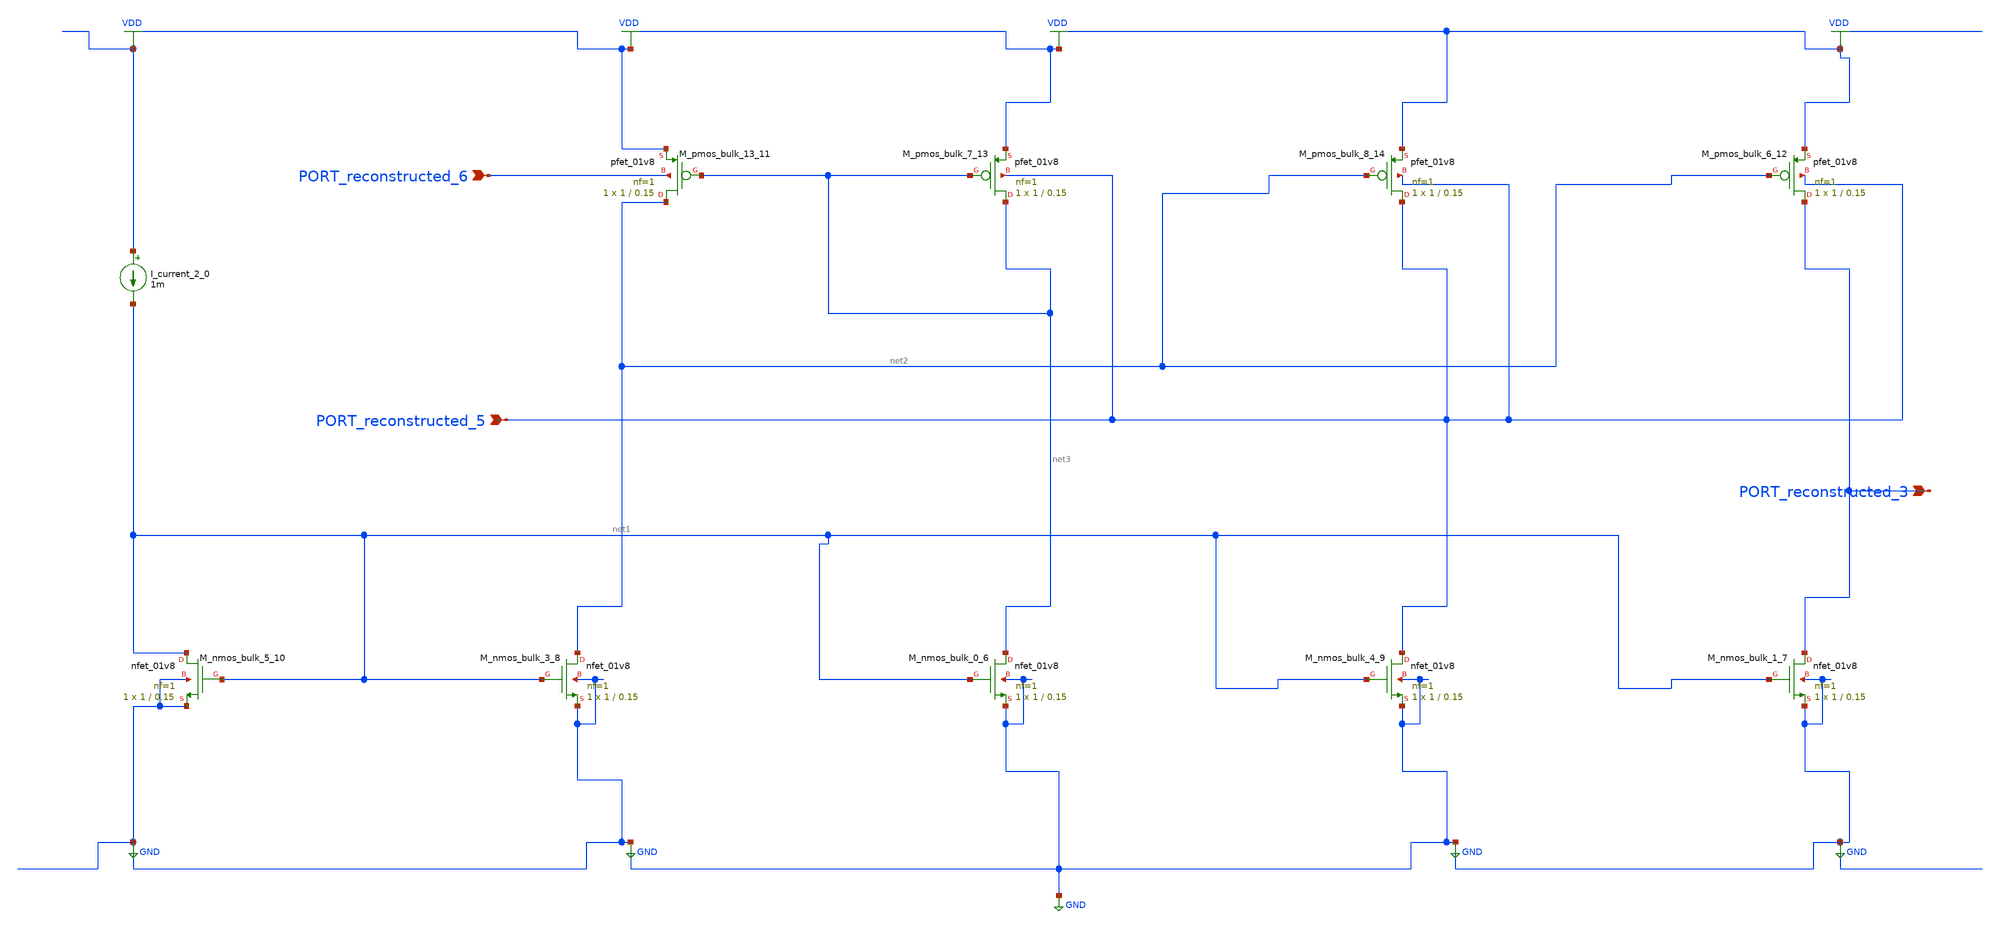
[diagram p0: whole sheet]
** sch_path: schematics/10_1051_e3sconf_202235101017_02_001.sch
**.subckt 10_1051_e3sconf_202235101017_02_001 PORT_reconstructed_5 PORT_reconstructed_6
*+ PORT_reconstructed_3
*.ipin PORT_reconstructed_5
*.ipin PORT_reconstructed_6
*.ipin PORT_reconstructed_3
I_current_2_0 VDD net1 1m
XM_nmos_bulk_0_6 net3 net1 GND GND sky130_fd_pr__nfet_01v8 L=0.15 W=1 nf=1 ad='int((1 + 1)/2) * 1 / 1 * 0.29'
+ as='int((1 + 2)/2) * 1 / 1 * 0.29' pd='2*int((1 + 1)/2) * (1 / 1 + 0.29)' ps='2*int((1 + 2)/2) * (1 / 1 + 0.29)'
+ nrd='0.29 / 1 ' nrs='0.29 / 1 ' sa=0 sb=0 sd=0 mult=1 m=1
XM_nmos_bulk_1_7 PORT_reconstructed_3 net1 GND GND sky130_fd_pr__nfet_01v8 L=0.15 W=1 nf=1 ad='int((1 + 1)/2) * 1 / 1 * 0.29'
+ as='int((1 + 2)/2) * 1 / 1 * 0.29' pd='2*int((1 + 1)/2) * (1 / 1 + 0.29)' ps='2*int((1 + 2)/2) * (1 / 1 + 0.29)'
+ nrd='0.29 / 1 ' nrs='0.29 / 1 ' sa=0 sb=0 sd=0 mult=1 m=1
XM_nmos_bulk_3_8 net2 net1 GND GND sky130_fd_pr__nfet_01v8 L=0.15 W=1 nf=1 ad='int((1 + 1)/2) * 1 / 1 * 0.29'
+ as='int((1 + 2)/2) * 1 / 1 * 0.29' pd='2*int((1 + 1)/2) * (1 / 1 + 0.29)' ps='2*int((1 + 2)/2) * (1 / 1 + 0.29)'
+ nrd='0.29 / 1 ' nrs='0.29 / 1 ' sa=0 sb=0 sd=0 mult=1 m=1
XM_nmos_bulk_4_9 PORT_reconstructed_5 net1 GND GND sky130_fd_pr__nfet_01v8 L=0.15 W=1 nf=1 ad='int((1 + 1)/2) * 1 / 1 * 0.29'
+ as='int((1 + 2)/2) * 1 / 1 * 0.29' pd='2*int((1 + 1)/2) * (1 / 1 + 0.29)' ps='2*int((1 + 2)/2) * (1 / 1 + 0.29)'
+ nrd='0.29 / 1 ' nrs='0.29 / 1 ' sa=0 sb=0 sd=0 mult=1 m=1
XM_nmos_bulk_5_10 net1 net1 GND GND sky130_fd_pr__nfet_01v8 L=0.15 W=1 nf=1 ad='int((1 + 1)/2) * 1 / 1 * 0.29'
+ as='int((1 + 2)/2) * 1 / 1 * 0.29' pd='2*int((1 + 1)/2) * (1 / 1 + 0.29)' ps='2*int((1 + 2)/2) * (1 / 1 + 0.29)'
+ nrd='0.29 / 1 ' nrs='0.29 / 1 ' sa=0 sb=0 sd=0 mult=1 m=1
XM_pmos_bulk_13_11 net2 net3 VDD PORT_reconstructed_6 sky130_fd_pr__pfet_01v8 L=0.15 W=1 nf=1 ad='int((1 + 1)/2) * 1 / 1 * 0.29'
+ as='int((1 + 2)/2) * 1 / 1 * 0.29' pd='2*int((1 + 1)/2) * (1 / 1 + 0.29)' ps='2*int((1 + 2)/2) * (1 / 1 + 0.29)'
+ nrd='0.29 / 1 ' nrs='0.29 / 1 ' sa=0 sb=0 sd=0 mult=1 m=1
XM_pmos_bulk_6_12 PORT_reconstructed_3 net2 VDD PORT_reconstructed_5 sky130_fd_pr__pfet_01v8 L=0.15 W=1
+ nf=1 ad='int((1 + 1)/2) * 1 / 1 * 0.29' as='int((1 + 2)/2) * 1 / 1 * 0.29' pd='2*int((1 + 1)/2) * (1 / 1 + 0.29)'
+ ps='2*int((1 + 2)/2) * (1 / 1 + 0.29)' nrd='0.29 / 1 ' nrs='0.29 / 1 ' sa=0 sb=0 sd=0 mult=1 m=1
XM_pmos_bulk_7_13 net3 net3 VDD PORT_reconstructed_5 sky130_fd_pr__pfet_01v8 L=0.15 W=1 nf=1 ad='int((1 + 1)/2) * 1 / 1 * 0.29'
+ as='int((1 + 2)/2) * 1 / 1 * 0.29' pd='2*int((1 + 1)/2) * (1 / 1 + 0.29)' ps='2*int((1 + 2)/2) * (1 / 1 + 0.29)'
+ nrd='0.29 / 1 ' nrs='0.29 / 1 ' sa=0 sb=0 sd=0 mult=1 m=1
XM_pmos_bulk_8_14 PORT_reconstructed_5 net2 VDD PORT_reconstructed_5 sky130_fd_pr__pfet_01v8 L=0.15 W=1
+ nf=1 ad='int((1 + 1)/2) * 1 / 1 * 0.29' as='int((1 + 2)/2) * 1 / 1 * 0.29' pd='2*int((1 + 1)/2) * (1 / 1 + 0.29)'
+ ps='2*int((1 + 2)/2) * (1 / 1 + 0.29)' nrd='0.29 / 1 ' nrs='0.29 / 1 ' sa=0 sb=0 sd=0 mult=1 m=1
**.ends
.GLOBAL GND
.GLOBAL VDD
.end
